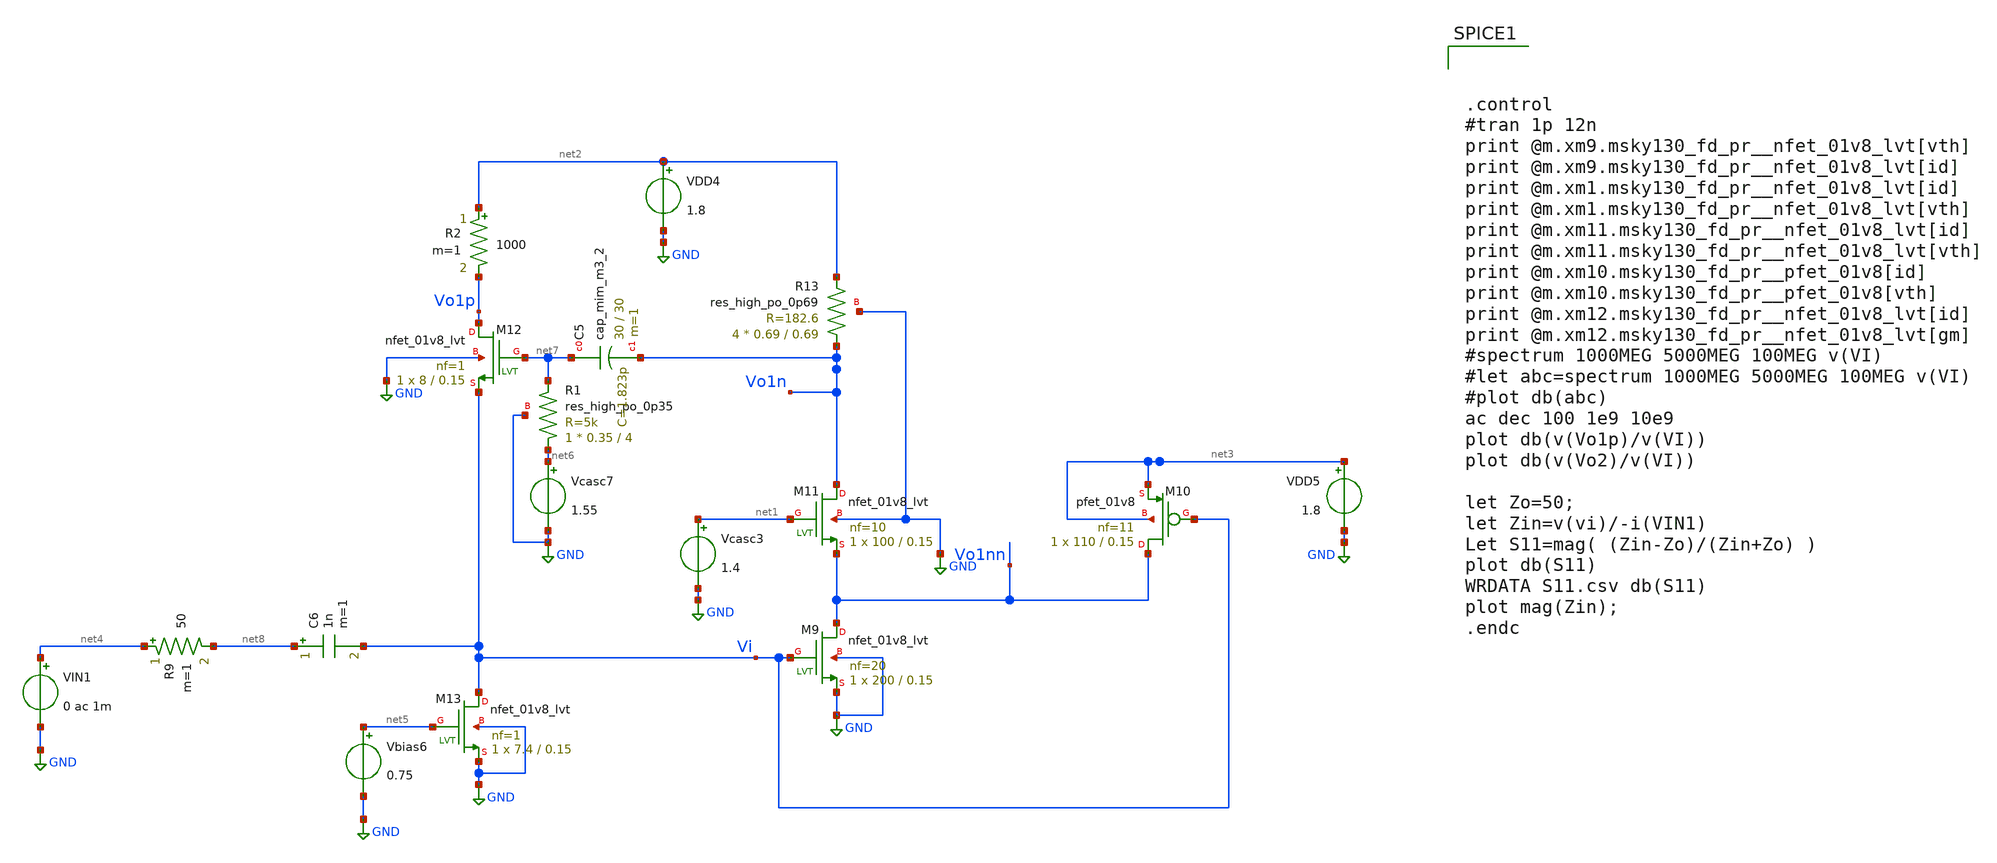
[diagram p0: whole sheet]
** sch_path: xschem/xschem4_sic_final/Com_amp_ac.sch
**.subckt Com_amp_ac
VIN1 net4 GND 0 ac 1m
Vcasc3 net1 GND 1.4
VDD4 net2 GND 1.8
VDD5 net3 GND 1.8
Vbias6 net5 GND 0.75
Vcasc7 net6 GND 1.55
XR1 net6 net7 GND sky130_fd_pr__res_high_po_0p35 L=4 mult=1 m=1
XC5 net7 Vo1n sky130_fd_pr__cap_mim_m3_2 W=30 L=30 MF=1 m=1
C6 net8 Vi 1n m=1
XM9 Vo1nn Vi GND GND sky130_fd_pr__nfet_01v8_lvt L=0.15 W=200 nf=20 ad='int((nf+1)/2) * W/nf * 0.29'
+ as='int((nf+2)/2) * W/nf * 0.29' pd='2*int((nf+1)/2) * (W/nf + 0.29)' ps='2*int((nf+2)/2) * (W/nf + 0.29)'
+ nrd='0.29 / W' nrs='0.29 / W' sa=0 sb=0 sd=0 mult=1 m=1
XM10 Vo1nn Vi net3 net3 sky130_fd_pr__pfet_01v8 L=0.15 W=110 nf=11 ad='int((nf+1)/2) * W/nf * 0.29' as='int((nf+2)/2) * W/nf * 0.29'
+ pd='2*int((nf+1)/2) * (W/nf + 0.29)' ps='2*int((nf+2)/2) * (W/nf + 0.29)' nrd='0.29 / W' nrs='0.29 / W'
+ sa=0 sb=0 sd=0 mult=1 m=1
XM11 Vo1n net1 Vo1nn GND sky130_fd_pr__nfet_01v8_lvt L=0.15 W=100 nf=10 ad='int((nf+1)/2) * W/nf * 0.29'
+ as='int((nf+2)/2) * W/nf * 0.29' pd='2*int((nf+1)/2) * (W/nf + 0.29)' ps='2*int((nf+2)/2) * (W/nf + 0.29)'
+ nrd='0.29 / W' nrs='0.29 / W' sa=0 sb=0 sd=0 mult=1 m=1
XM12 Vo1p net7 Vi GND sky130_fd_pr__nfet_01v8_lvt L=0.15 W=8 nf=1 ad='int((nf+1)/2) * W/nf * 0.29' as='int((nf+2)/2) * W/nf * 0.29'
+ pd='2*int((nf+1)/2) * (W/nf + 0.29)' ps='2*int((nf+2)/2) * (W/nf + 0.29)' nrd='0.29 / W' nrs='0.29 / W'
+ sa=0 sb=0 sd=0 mult=1 m=1
XM13 Vi net5 GND GND sky130_fd_pr__nfet_01v8_lvt L=0.15 W=7.4 nf=1 ad='int((nf+1)/2) * W/nf * 0.29' as='int((nf+2)/2) * W/nf * 0.29'
+ pd='2*int((nf+1)/2) * (W/nf + 0.29)' ps='2*int((nf+2)/2) * (W/nf + 0.29)' nrd='0.29 / W' nrs='0.29 / W'
+ sa=0 sb=0 sd=0 mult=1 m=1
R9 net4 net8 50 m=1
XR13 Vo1n net2 GND sky130_fd_pr__res_high_po_0p69 L=0.69 mult=4 m=4
R2 net2 Vo1p 1000 m=1
**** begin user architecture code

.lib $::SKYWATER_MODELS/sky130.lib.spice tt




.control
#tran 1p 12n
print @m.xm9.msky130_fd_pr__nfet_01v8_lvt[vth]
print @m.xm9.msky130_fd_pr__nfet_01v8_lvt[id]
print @m.xm1.msky130_fd_pr__nfet_01v8_lvt[id]
print @m.xm1.msky130_fd_pr__nfet_01v8_lvt[vth]
print @m.xm11.msky130_fd_pr__nfet_01v8_lvt[id]
print @m.xm11.msky130_fd_pr__nfet_01v8_lvt[vth]
print @m.xm10.msky130_fd_pr__pfet_01v8[id]
print @m.xm10.msky130_fd_pr__pfet_01v8[vth]
print @m.xm12.msky130_fd_pr__nfet_01v8_lvt[id]
print @m.xm12.msky130_fd_pr__nfet_01v8_lvt[gm]
#spectrum 1000MEG 5000MEG 100MEG v(VI)
#let abc=spectrum 1000MEG 5000MEG 100MEG v(VI)
#plot db(abc)
ac dec 100 1e9 10e9
plot db(v(Vo1p)/v(VI))
plot db(v(Vo2)/v(VI))

let Zo=50;
let Zin=v(vi)/-i(VIN1)
Let S11=mag( (Zin-Zo)/(Zin+Zo) )
plot db(S11)
WRDATA S11.csv db(S11)
plot mag(Zin);
.endc


**** end user architecture code
**.ends
.GLOBAL GND
.end
